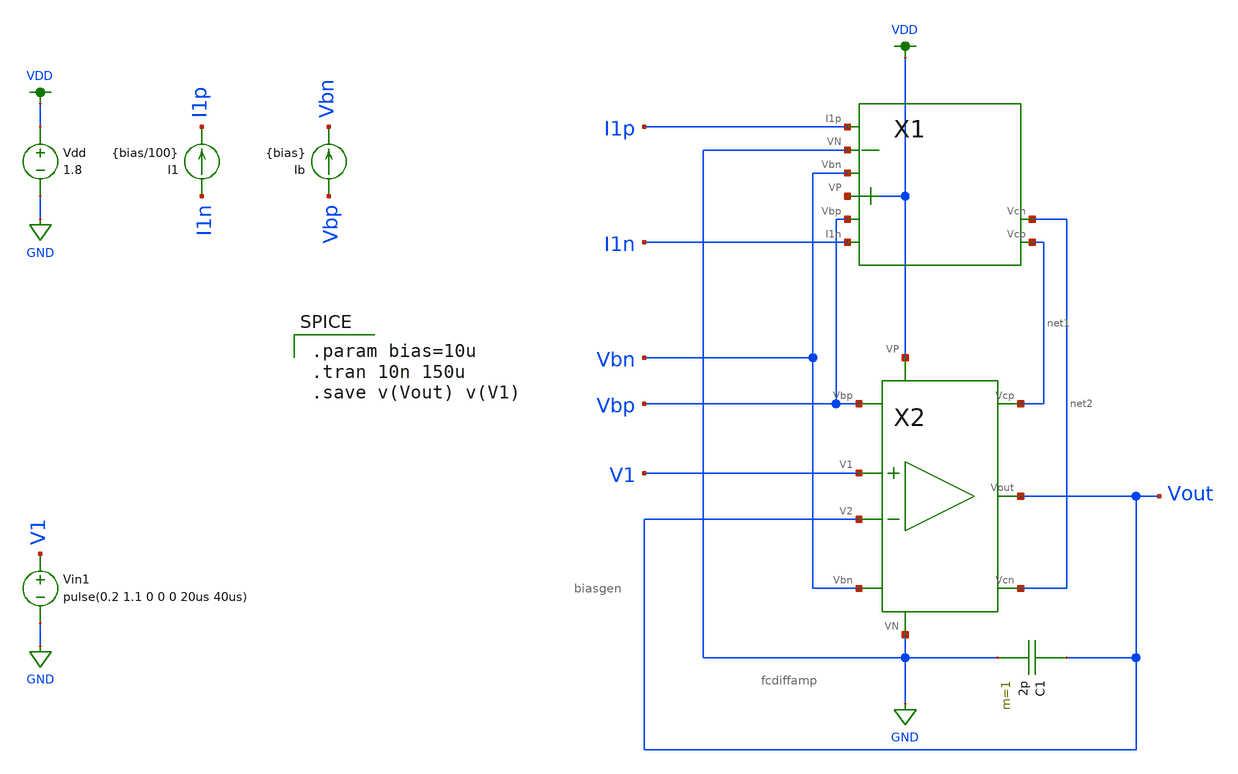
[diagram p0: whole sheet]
** sch_path: full_fcdiff_test.sch
**.subckt full_fcdiff_test
X1 I1n Vbp VDD Vbn GND I1p net1 net2 biasgen
X2 Vbp V1 Vout Vbn GND net2 net1 VDD Vout fcdiffamp
Vdd VDD GND 1.8
I1 I1n I1p {bias/100}
Ib Vbp Vbn {bias}
Vin1 V1 GND pulse(0.2 1.1 0 0 0 20us 40us)
C1 Vout GND 2p m=1
**** begin user architecture code

.param bias=10u
.tran 10n 150u
.save v(Vout) v(V1)


.option wnflag=1
.lib ~/skywater/skywater-pdk/libraries/sky130_fd_pr_ngspice/latest/models/sky130.lib.spice tt

**** end user architecture code
**.ends
.GLOBAL VDD
.GLOBAL GND
.end
